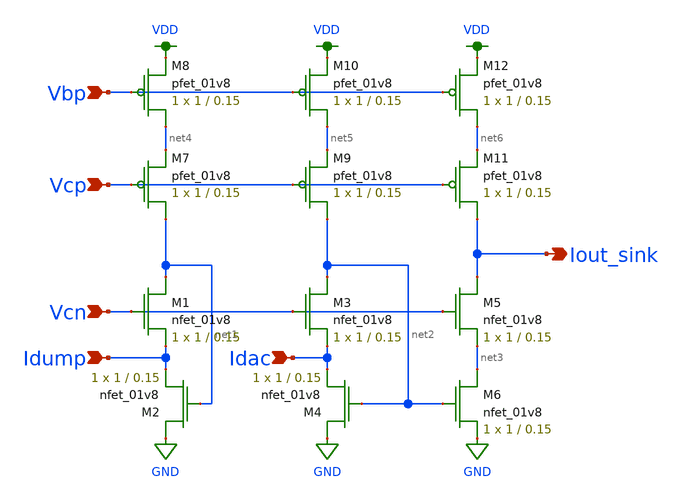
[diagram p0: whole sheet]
** sch_path: output_sink.sch
**.subckt output_sink Idump Idac Vcn Vcp Vbp Iout_sink
*.ipin Idump
*.ipin Idac
*.ipin Vcn
*.ipin Vcp
*.ipin Vbp
*.opin Iout_sink
XM1 net1 Vcn Idump GND sky130_fd_pr__nfet_01v8 L=0.15 W=1 nf=1 ad='int((nf+1)/2) * W/nf * 0.29' as='int((nf+2)/2) * W/nf * 0.29'
+ pd='2*int((nf+1)/2) * (W/nf + 0.29)' ps='2*int((nf+2)/2) * (W/nf + 0.29)' nrd='0.29 / W' nrs='0.29 / W'
+ sa=0 sb=0 sd=0 mult=1 m=1
XM2 GND net1 Idump GND sky130_fd_pr__nfet_01v8 L=0.15 W=1 nf=1 ad='int((nf+1)/2) * W/nf * 0.29' as='int((nf+2)/2) * W/nf * 0.29'
+ pd='2*int((nf+1)/2) * (W/nf + 0.29)' ps='2*int((nf+2)/2) * (W/nf + 0.29)' nrd='0.29 / W' nrs='0.29 / W'
+ sa=0 sb=0 sd=0 mult=1 m=1
XM3 net2 Vcn Idac GND sky130_fd_pr__nfet_01v8 L=0.15 W=1 nf=1 ad='int((nf+1)/2) * W/nf * 0.29' as='int((nf+2)/2) * W/nf * 0.29'
+ pd='2*int((nf+1)/2) * (W/nf + 0.29)' ps='2*int((nf+2)/2) * (W/nf + 0.29)' nrd='0.29 / W' nrs='0.29 / W'
+ sa=0 sb=0 sd=0 mult=1 m=1
XM4 GND net2 Idac GND sky130_fd_pr__nfet_01v8 L=0.15 W=1 nf=1 ad='int((nf+1)/2) * W/nf * 0.29' as='int((nf+2)/2) * W/nf * 0.29'
+ pd='2*int((nf+1)/2) * (W/nf + 0.29)' ps='2*int((nf+2)/2) * (W/nf + 0.29)' nrd='0.29 / W' nrs='0.29 / W'
+ sa=0 sb=0 sd=0 mult=1 m=1
XM5 Iout_sink Vcn net3 GND sky130_fd_pr__nfet_01v8 L=0.15 W=1 nf=1 ad='int((nf+1)/2) * W/nf * 0.29' as='int((nf+2)/2) * W/nf * 0.29'
+ pd='2*int((nf+1)/2) * (W/nf + 0.29)' ps='2*int((nf+2)/2) * (W/nf + 0.29)' nrd='0.29 / W' nrs='0.29 / W'
+ sa=0 sb=0 sd=0 mult=1 m=1
XM6 net3 net2 GND GND sky130_fd_pr__nfet_01v8 L=0.15 W=1 nf=1 ad='int((nf+1)/2) * W/nf * 0.29' as='int((nf+2)/2) * W/nf * 0.29'
+ pd='2*int((nf+1)/2) * (W/nf + 0.29)' ps='2*int((nf+2)/2) * (W/nf + 0.29)' nrd='0.29 / W' nrs='0.29 / W'
+ sa=0 sb=0 sd=0 mult=1 m=1
XM7 net1 Vcp net4 VDD sky130_fd_pr__pfet_01v8 L=0.15 W=1 nf=1 ad='int((nf+1)/2) * W/nf * 0.29' as='int((nf+2)/2) * W/nf * 0.29'
+ pd='2*int((nf+1)/2) * (W/nf + 0.29)' ps='2*int((nf+2)/2) * (W/nf + 0.29)' nrd='0.29 / W' nrs='0.29 / W'
+ sa=0 sb=0 sd=0 mult=1 m=1
XM8 net4 Vbp VDD VDD sky130_fd_pr__pfet_01v8 L=0.15 W=1 nf=1 ad='int((nf+1)/2) * W/nf * 0.29' as='int((nf+2)/2) * W/nf * 0.29'
+ pd='2*int((nf+1)/2) * (W/nf + 0.29)' ps='2*int((nf+2)/2) * (W/nf + 0.29)' nrd='0.29 / W' nrs='0.29 / W'
+ sa=0 sb=0 sd=0 mult=1 m=1
XM9 net2 Vcp net5 VDD sky130_fd_pr__pfet_01v8 L=0.15 W=1 nf=1 ad='int((nf+1)/2) * W/nf * 0.29' as='int((nf+2)/2) * W/nf * 0.29'
+ pd='2*int((nf+1)/2) * (W/nf + 0.29)' ps='2*int((nf+2)/2) * (W/nf + 0.29)' nrd='0.29 / W' nrs='0.29 / W'
+ sa=0 sb=0 sd=0 mult=1 m=1
XM10 net5 Vbp VDD VDD sky130_fd_pr__pfet_01v8 L=0.15 W=1 nf=1 ad='int((nf+1)/2) * W/nf * 0.29' as='int((nf+2)/2) * W/nf * 0.29'
+ pd='2*int((nf+1)/2) * (W/nf + 0.29)' ps='2*int((nf+2)/2) * (W/nf + 0.29)' nrd='0.29 / W' nrs='0.29 / W'
+ sa=0 sb=0 sd=0 mult=1 m=1
XM11 Iout_sink Vcp net6 VDD sky130_fd_pr__pfet_01v8 L=0.15 W=1 nf=1 ad='int((nf+1)/2) * W/nf * 0.29'
+ as='int((nf+2)/2) * W/nf * 0.29' pd='2*int((nf+1)/2) * (W/nf + 0.29)' ps='2*int((nf+2)/2) * (W/nf + 0.29)'
+ nrd='0.29 / W' nrs='0.29 / W' sa=0 sb=0 sd=0 mult=1 m=1
XM12 net6 Vbp VDD VDD sky130_fd_pr__pfet_01v8 L=0.15 W=1 nf=1 ad='int((nf+1)/2) * W/nf * 0.29' as='int((nf+2)/2) * W/nf * 0.29'
+ pd='2*int((nf+1)/2) * (W/nf + 0.29)' ps='2*int((nf+2)/2) * (W/nf + 0.29)' nrd='0.29 / W' nrs='0.29 / W'
+ sa=0 sb=0 sd=0 mult=1 m=1
**.ends
.GLOBAL GND
.GLOBAL VDD
.end
